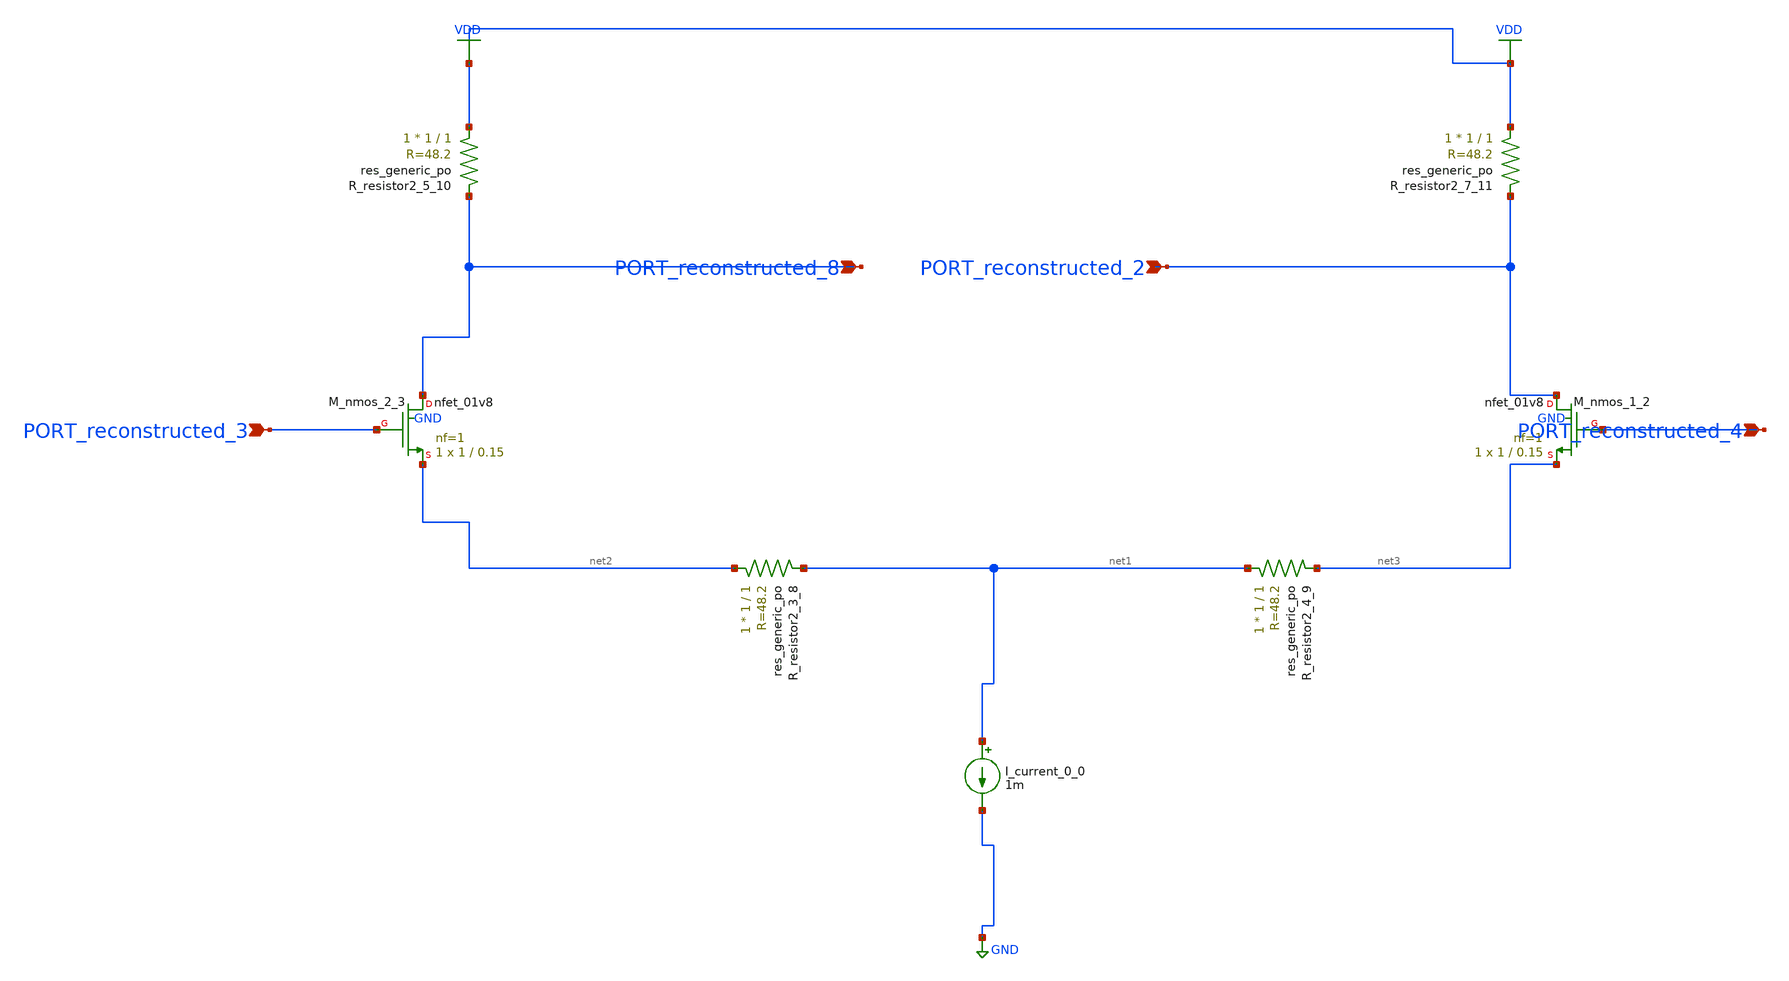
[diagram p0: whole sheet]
** sch_path: schematics/AMSNet/247.sch
**.subckt 247 PORT_reconstructed_8 PORT_reconstructed_2 PORT_reconstructed_3 PORT_reconstructed_4
*.ipin PORT_reconstructed_8
*.ipin PORT_reconstructed_2
*.ipin PORT_reconstructed_3
*.ipin PORT_reconstructed_4
I_current_0_0 net1 GND 1m
XM_nmos_1_2 PORT_reconstructed_2 PORT_reconstructed_4 net3 GND sky130_fd_pr__nfet_01v8 L=0.15 W=1 nf=1
+ ad='int((1 + 1)/2) * 1 / 1 * 0.29' as='int((1 + 2)/2) * 1 / 1 * 0.29' pd='2*int((1 + 1)/2) * (1 / 1 + 0.29)'
+ ps='2*int((1 + 2)/2) * (1 / 1 + 0.29)' nrd='0.29 / 1 ' nrs='0.29 / 1 ' sa=0 sb=0 sd=0 mult=1 m=1
XM_nmos_2_3 PORT_reconstructed_8 PORT_reconstructed_3 net2 GND sky130_fd_pr__nfet_01v8 L=0.15 W=1 nf=1
+ ad='int((1 + 1)/2) * 1 / 1 * 0.29' as='int((1 + 2)/2) * 1 / 1 * 0.29' pd='2*int((1 + 1)/2) * (1 / 1 + 0.29)'
+ ps='2*int((1 + 2)/2) * (1 / 1 + 0.29)' nrd='0.29 / 1 ' nrs='0.29 / 1 ' sa=0 sb=0 sd=0 mult=1 m=1
XR_resistor2_3_8 net2 net1 sky130_fd_pr__res_generic_po W=1 L=1 m=1
XR_resistor2_4_9 net1 net3 sky130_fd_pr__res_generic_po W=1 L=1 m=1
XR_resistor2_5_10 VDD PORT_reconstructed_8 sky130_fd_pr__res_generic_po W=1 L=1 m=1
XR_resistor2_7_11 VDD PORT_reconstructed_2 sky130_fd_pr__res_generic_po W=1 L=1 m=1
**.ends
.GLOBAL GND
.GLOBAL VDD
.end
